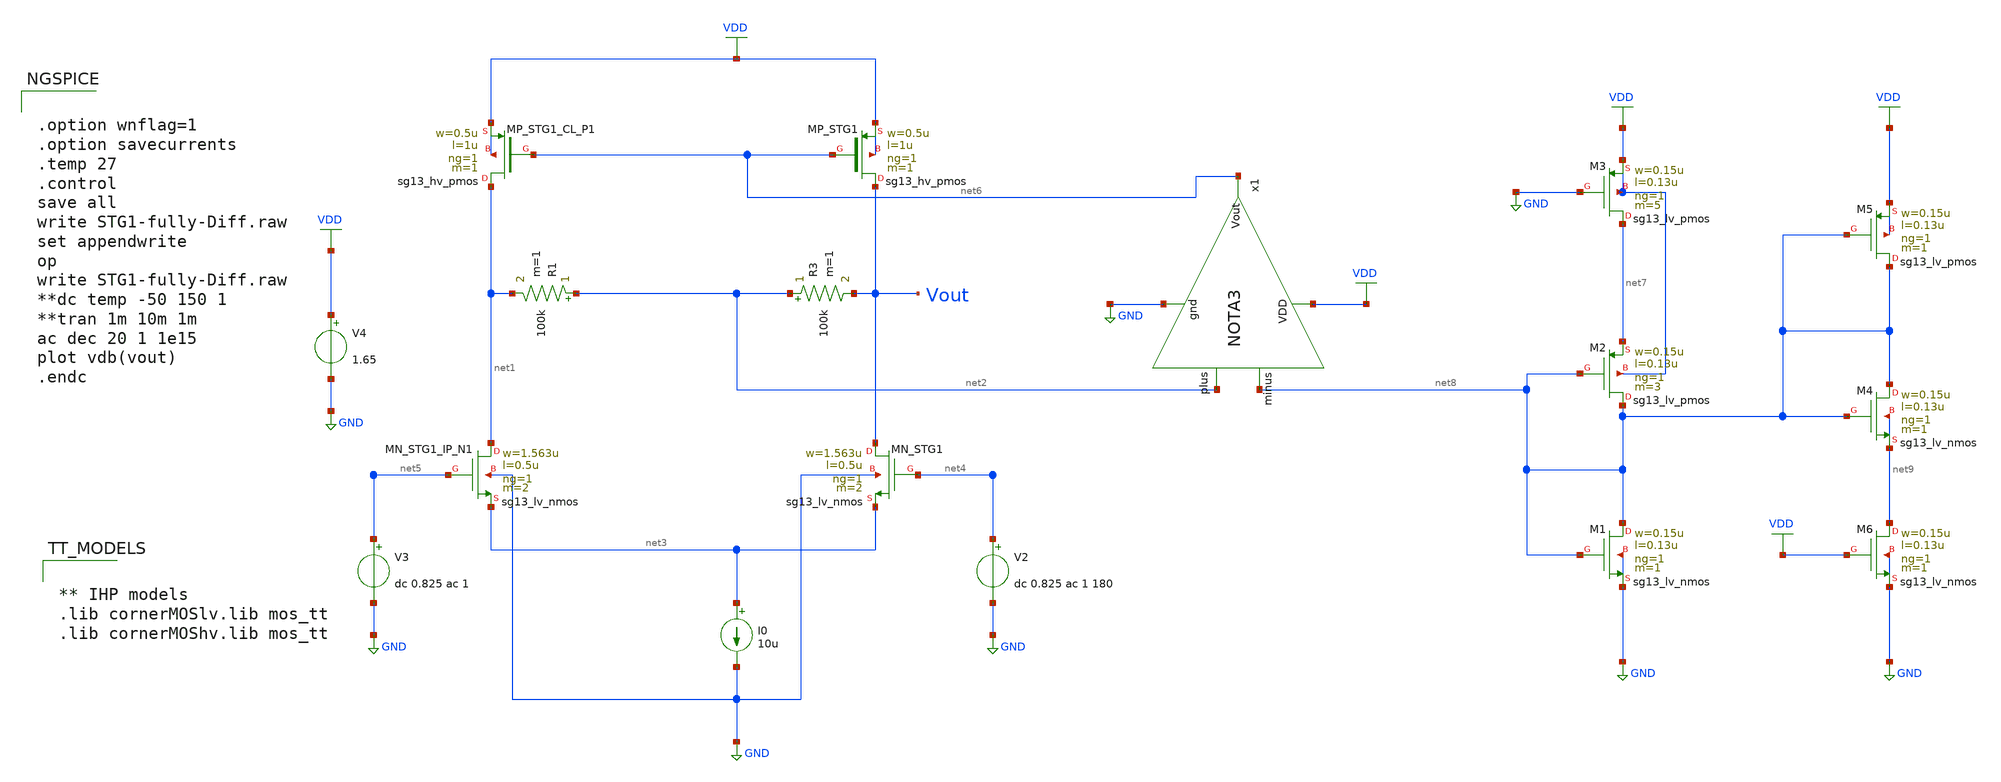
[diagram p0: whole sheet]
** sch_path: Design Files/RAMP/STG1-fully-Diff.sch
**.subckt STG1-fully-Diff
R1 net2 net1 100k m=1
R3 net2 Vout 100k m=1
I0 net3 GND 10u
V2 net4 GND dc 0.825 ac 1 180
V3 net5 GND dc 0.825 ac 1
V4 VDD GND 1.65
XM1 net8 net8 GND GND sg13_lv_nmos w=0.15u l=0.13u ng=1 m=1 mm_ok=1
XM2 net8 net8 net7 VDD sg13_lv_pmos w=0.15u l=0.13u ng=1 m=3 mm_ok=1
XM3 net7 GND VDD VDD sg13_lv_pmos w=0.15u l=0.13u ng=1 m=5 mm_ok=1
XM4 net8 net8 net9 net9 sg13_lv_nmos w=0.15u l=0.13u ng=1 m=1 mm_ok=1
XM5 net8 net8 VDD VDD sg13_lv_pmos w=0.15u l=0.13u ng=1 m=1 mm_ok=1
XM6 net9 VDD GND GND sg13_lv_nmos w=0.15u l=0.13u ng=1 m=1 mm_ok=1
XMP_STG1_CL_P1 net1 net6 VDD VDD sg13_hv_pmos w=0.5u l=1u ng=1 m=1 mm_ok=1
XMP_STG1 Vout net6 VDD VDD sg13_hv_pmos w=0.5u l=1u ng=1 m=1 mm_ok=1
XMN_STG1_IP_N1 net1 net5 net3 GND sg13_lv_nmos w=1.563u l=0.5u ng=1 m=2 mm_ok=1
XMN_STG1 Vout net4 net3 GND sg13_lv_nmos w=1.563u l=0.5u ng=1 m=2 mm_ok=1
x1 VDD net6 net8 net2 GND NOTA3
**** begin user architecture code


.option wnflag=1
.option savecurrents
.temp 27
.control
save all
write STG1-fully-Diff.raw
set appendwrite
op
write STG1-fully-Diff.raw
**dc temp -50 150 1
**tran 1m 10m 1m
ac dec 20 1 1e15
plot vdb(vout)
.endc




** IHP models
.lib cornerMOSlv.lib mos_tt
.lib cornerMOShv.lib mos_tt




.save @n.xip_stg1_mn1.nsg13_lv_nmos[gds]
.save @n.xip_stg1_mn1.nsg13_lv_nmos[gm]
.save @n.xip_stg1_mn1.nsg13_lv_nmos[gmb]
.save @n.xip_stg1_mn1.nsg13_lv_nmos[ids]
.save @n.xip_stg1_mn1.nsg13_lv_nmos[l]
.save @n.xip_stg1_mn1.nsg13_lv_nmos[vgs]
.save @n.xip_stg1_mn1.nsg13_lv_nmos[vth]
.save @n.xip_stg1_mn1.nsg13_lv_nmos[vds]
.save @n.xip_stg1_mn1.nsg13_lv_nmos[cgg]
.save @n.xip_stg1_mn1.nsg13_lv_nmos[vsat]
.save @n.xip_stg1_mn1.nsg13_lv_nmos[cgd]
.save @n.xip_stg1_mn1.nsg13_lv_nmos[cgs]
.save @n.xip_stg1_mn2.nsg13_lv_nmos[gds]
.save @n.xip_stg1_mn2.nsg13_lv_nmos[gm]
.save @n.xip_stg1_mn2.nsg13_lv_nmos[gmb]
.save @n.xip_stg1_mn2.nsg13_lv_nmos[ids]
.save @n.xip_stg1_mn2.nsg13_lv_nmos[l]
.save @n.xip_stg1_mn2.nsg13_lv_nmos[vth]
.save @n.xip_stg1_mn2.nsg13_lv_nmos[vsat]
.save @n.xip_stg1_mn2.nsg13_lv_nmos[vgs]
.save @n.xip_stg1_mn2.nsg13_lv_nmos[vds]
.save @n.xip_stg1_mn2.nsg13_lv_nmos[cgd]
.save @n.xip_stg1_mn2.nsg13_lv_nmos[cgs]
.save @n.xip_stg1_mn2.nsg13_lv_nmos[cgg]
.save @n.xip_stg1_mn2.nsg13_lv_nmos[gds]

.save @n.xmp_stg1_cl_p1.nsg13_hv_pmos[gds]
.save @n.xmp_stg1_cl_p1.nsg13_hv_pmos[gm]
.save @n.xmp_stg1_cl_p1.nsg13_hv_pmos[gmb]
.save @n.xmp_stg1_cl_p1.nsg13_hv_pmos[ids]
.save @n.xmp_stg1_cl_p1.nsg13_hv_pmos[l]
.save @n.xmp_stg1_cl_p1.nsg13_hv_pmos[vth]
.save @n.xmp_stg1_cl_p1.nsg13_hv_pmos[vsat]
.save @n.xmp_stg1_cl_p1.nsg13_hv_pmos[vgs]
.save @n.xmp_stg1_cl_p1.nsg13_hv_pmos[vds]
.save @n.xmp_stg1_cl_p1.nsg13_hv_pmos[cgd]
.save @n.xmp_stg1_cl_p1.nsg13_hv_pmos[cgs]
.save @n.xmp_stg1_cl_p1.nsg13_hv_pmos[cgg]
.save @n.xmp_stg1_cl_p1.nsg13_hv_pmos[gds]
.save @n.xmp_stg1_cl_p2.nsg13_hv_pmos[gds]
.save @n.xmp_stg1_cl_p2.nsg13_hv_pmos[gm]
.save @n.xmp_stg1_cl_p2.nsg13_hv_pmos[gmb]
.save @n.xmp_stg1_cl_p2.nsg13_hv_pmos[ids]
.save @n.xmp_stg1_cl_p2.nsg13_hv_pmos[l]
.save @n.xmp_stg1_cl_p2.nsg13_hv_pmos[vth]
.save @n.xmp_stg1_cl_p2.nsg13_hv_pmos[vsat]
.save @n.xmp_stg1_cl_p2.nsg13_hv_pmos[vgs]
.save @n.xmp_stg1_cl_p2.nsg13_hv_pmos[vds]
.save @n.xmp_stg1_cl_p2.nsg13_hv_pmos[cgd]
.save @n.xmp_stg1_cl_p2.nsg13_hv_pmos[cgs]
.save @n.xmp_stg1_cl_p2.nsg13_hv_pmos[cgg]
.save @n.xmp_stg1_cl_p2.nsg13_hv_pmos[gds]


**** end user architecture code
**.ends

* expanding   symbol:  /foss/designs/RAMP/OTA/NOTA3.sym # of pins=5
** sym_path: Design Files/RAMP/OTA/NOTA3.sym
** sch_path: Design Files/RAMP/OTA/NOTA3.sch
.subckt NOTA3 VDD Vout minus plus gnd
*.ipin plus
*.ipin minus
*.ipin VDD
*.ipin gnd
*.opin Vout
XM1 net2 plus net1 gnd sg13_hv_nmos w=3.25u l=1.5u ng=1 m=2 mm_ok=1
XM2 Vout minus net1 gnd sg13_hv_nmos w=3.25u l=1.5u ng=1 m=2 mm_ok=1
XM3 Vout net2 VDD VDD sg13_hv_pmos w=2u l=2u ng=1 m=1 mm_ok=1
XM4 net2 net2 VDD VDD sg13_hv_pmos w=2u l=2u ng=1 m=1 mm_ok=1
I0 net1 gnd 2u
.ends

.GLOBAL GND
.GLOBAL VDD
.end
